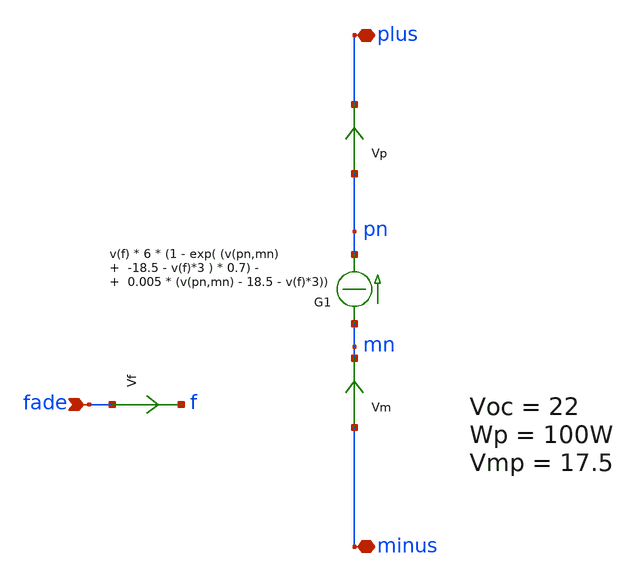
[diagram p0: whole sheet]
** sch_path: xschem_library/ngspice/pv_ngspice.sch
**.subckt pv_ngspice plus minus fade
*.iopin plus
*.iopin minus
*.ipin fade
Vm minus mn 0
.save i(vm)
G1 mn pn CUR=' v(f) * 6 * (1 - exp( (v(pn,mn) -18.5 - v(f)*3 ) * 0.7) - 0.005 * (v(pn,mn) - 18.5 - v(f)*3)) '
Vf fade f 0
.save i(vf)
Vp pn plus 0
.save i(vp)
**.ends
.end
